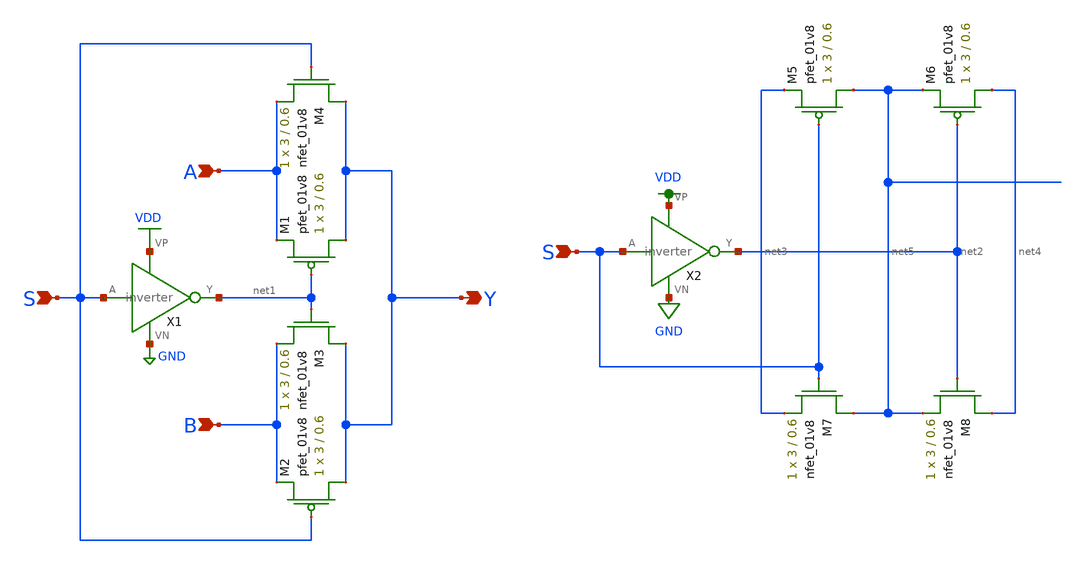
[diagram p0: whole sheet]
** sch_path: schematic/LDS/mux2.sch
**.subckt mux2 Y B A S S
*.opin Y
*.ipin B
*.ipin A
*.ipin S
*.ipin S
XM1 Y net1 A VDD sky130_fd_pr__pfet_01v8 L=0.6 W=3 nf=1 ad='int((nf+1)/2) * W/nf * 0.29' as='int((nf+2)/2) * W/nf * 0.29'
+ pd='2*int((nf+1)/2) * (W/nf + 0.29)' ps='2*int((nf+2)/2) * (W/nf + 0.29)' nrd='0.29 / W' nrs='0.29 / W'
+ sa=0 sb=0 sd=0 mult=1 m=1
XM2 Y S B VDD sky130_fd_pr__pfet_01v8 L=0.6 W=3 nf=1 ad='int((nf+1)/2) * W/nf * 0.29' as='int((nf+2)/2) * W/nf * 0.29'
+ pd='2*int((nf+1)/2) * (W/nf + 0.29)' ps='2*int((nf+2)/2) * (W/nf + 0.29)' nrd='0.29 / W' nrs='0.29 / W'
+ sa=0 sb=0 sd=0 mult=1 m=1
XM3 Y net1 B GND sky130_fd_pr__nfet_01v8 L=0.6 W=3 nf=1 ad='int((nf+1)/2) * W/nf * 0.29' as='int((nf+2)/2) * W/nf * 0.29'
+ pd='2*int((nf+1)/2) * (W/nf + 0.29)' ps='2*int((nf+2)/2) * (W/nf + 0.29)' nrd='0.29 / W' nrs='0.29 / W'
+ sa=0 sb=0 sd=0 mult=1 m=1
XM4 Y S A GND sky130_fd_pr__nfet_01v8 L=0.6 W=3 nf=1 ad='int((nf+1)/2) * W/nf * 0.29' as='int((nf+2)/2) * W/nf * 0.29'
+ pd='2*int((nf+1)/2) * (W/nf + 0.29)' ps='2*int((nf+2)/2) * (W/nf + 0.29)' nrd='0.29 / W' nrs='0.29 / W'
+ sa=0 sb=0 sd=0 mult=1 m=1
X1 S net1 VDD GND inverter
X2 S net2 VDD GND inverter
XM5 net5 S net3 VDD sky130_fd_pr__pfet_01v8 L=0.6 W=3 nf=1 ad='int((nf+1)/2) * W/nf * 0.29' as='int((nf+2)/2) * W/nf * 0.29'
+ pd='2*int((nf+1)/2) * (W/nf + 0.29)' ps='2*int((nf+2)/2) * (W/nf + 0.29)' nrd='0.29 / W' nrs='0.29 / W'
+ sa=0 sb=0 sd=0 mult=1 m=1
XM6 net4 net2 net5 VDD sky130_fd_pr__pfet_01v8 L=0.6 W=3 nf=1 ad='int((nf+1)/2) * W/nf * 0.29' as='int((nf+2)/2) * W/nf * 0.29'
+ pd='2*int((nf+1)/2) * (W/nf + 0.29)' ps='2*int((nf+2)/2) * (W/nf + 0.29)' nrd='0.29 / W' nrs='0.29 / W'
+ sa=0 sb=0 sd=0 mult=1 m=1
XM7 net5 S net3 GND sky130_fd_pr__nfet_01v8 L=0.6 W=3 nf=1 ad='int((nf+1)/2) * W/nf * 0.29' as='int((nf+2)/2) * W/nf * 0.29'
+ pd='2*int((nf+1)/2) * (W/nf + 0.29)' ps='2*int((nf+2)/2) * (W/nf + 0.29)' nrd='0.29 / W' nrs='0.29 / W'
+ sa=0 sb=0 sd=0 mult=1 m=1
XM8 net4 net2 net5 GND sky130_fd_pr__nfet_01v8 L=0.6 W=3 nf=1 ad='int((nf+1)/2) * W/nf * 0.29' as='int((nf+2)/2) * W/nf * 0.29'
+ pd='2*int((nf+1)/2) * (W/nf + 0.29)' ps='2*int((nf+2)/2) * (W/nf + 0.29)' nrd='0.29 / W' nrs='0.29 / W'
+ sa=0 sb=0 sd=0 mult=1 m=1
**.ends

* expanding   symbol:  /home/madvlsi/Documents/MADVLSI-MP4/schematic/inverter.sym # of pins=4
** sym_path: /home/madvlsi/Documents/MADVLSI-MP4/schematic/inverter.sym
** sch_path: /home/madvlsi/Documents/MADVLSI-MP4/schematic/inverter.sch
.subckt inverter A Y VP VN
*.opin Y
*.ipin A
*.iopin VP
*.iopin VN
XM3 Y A VP VDD sky130_fd_pr__pfet_01v8 L=0.15 W=1 nf=1 ad='int((nf+1)/2) * W/nf * 0.29' as='int((nf+2)/2) * W/nf * 0.29'
+ pd='2*int((nf+1)/2) * (W/nf + 0.29)' ps='2*int((nf+2)/2) * (W/nf + 0.29)' nrd='0.29 / W' nrs='0.29 / W'
+ sa=0 sb=0 sd=0 mult=1 m=1
XM4 Y A VP VDD sky130_fd_pr__pfet_01v8 L=0.15 W=1 nf=1 ad='int((nf+1)/2) * W/nf * 0.29' as='int((nf+2)/2) * W/nf * 0.29'
+ pd='2*int((nf+1)/2) * (W/nf + 0.29)' ps='2*int((nf+2)/2) * (W/nf + 0.29)' nrd='0.29 / W' nrs='0.29 / W'
+ sa=0 sb=0 sd=0 mult=1 m=1
XM5 Y A VN GND sky130_fd_pr__nfet_01v8 L=0.15 W=1 nf=1 ad='int((nf+1)/2) * W/nf * 0.29' as='int((nf+2)/2) * W/nf * 0.29'
+ pd='2*int((nf+1)/2) * (W/nf + 0.29)' ps='2*int((nf+2)/2) * (W/nf + 0.29)' nrd='0.29 / W' nrs='0.29 / W'
+ sa=0 sb=0 sd=0 mult=1 m=1
.ends

.GLOBAL VDD
.GLOBAL GND
.end
